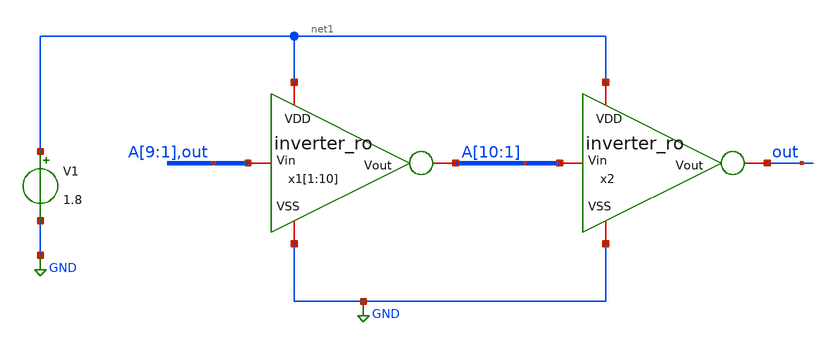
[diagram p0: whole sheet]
** sch_path: TT/ro_tb.sch
.lib $::SKYWATER_MODELS/sky130.lib.spice tt
.include $::SKYWATER_STDCELLS/sky130_fd_sc_hd.spice

**.subckt ro_tb
x1[1] net1 A[10] A[9] GND inverter_ro
x1[2] net1 A[9] A[8] GND inverter_ro
x1[3] net1 A[8] A[7] GND inverter_ro
x1[4] net1 A[7] A[6] GND inverter_ro
x1[5] net1 A[6] A[5] GND inverter_ro
x1[6] net1 A[5] A[4] GND inverter_ro
x1[7] net1 A[4] A[3] GND inverter_ro
x1[8] net1 A[3] A[2] GND inverter_ro
x1[9] net1 A[2] A[1] GND inverter_ro
x1[10] net1 A[1] out GND inverter_ro
x2 net1 out A[10] GND inverter_ro
V1 net1 GND 1.8
**** begin user architecture code


.ic V(out)=1.8
.tran 0.1n 50n
.save all



**** end user architecture code
**.ends

* expanding   symbol:  /foss/designs/Projects/RO_reliability/xschem/inverter_ro.sym # of pins=4
** sym_path: TT/inverter_ro.sym
** sch_path: TT/inverter_ro.sch
.subckt inverter_ro VDD Vout Vin VSS
*.iopin VDD
*.iopin VSS
*.iopin Vout
*.iopin Vin
XM1 Vout Vin VDD VDD sky130_fd_pr__pfet_01v8 L=0.15 W=1 nf=1 ad='int((nf+1)/2) * W/nf * 0.29' as='int((nf+2)/2) * W/nf * 0.29'
+ pd='2*int((nf+1)/2) * (W/nf + 0.29)' ps='2*int((nf+2)/2) * (W/nf + 0.29)' nrd='0.29 / W' nrs='0.29 / W'
+ sa=0 sb=0 sd=0 mult=1 m=1
XM2 Vout Vin VSS VSS sky130_fd_pr__nfet_01v8 L=0.15 W=1 nf=1 ad='int((nf+1)/2) * W/nf * 0.29' as='int((nf+2)/2) * W/nf * 0.29'
+ pd='2*int((nf+1)/2) * (W/nf + 0.29)' ps='2*int((nf+2)/2) * (W/nf + 0.29)' nrd='0.29 / W' nrs='0.29 / W'
+ sa=0 sb=0 sd=0 mult=1 m=1
.ends

.GLOBAL GND
.end
